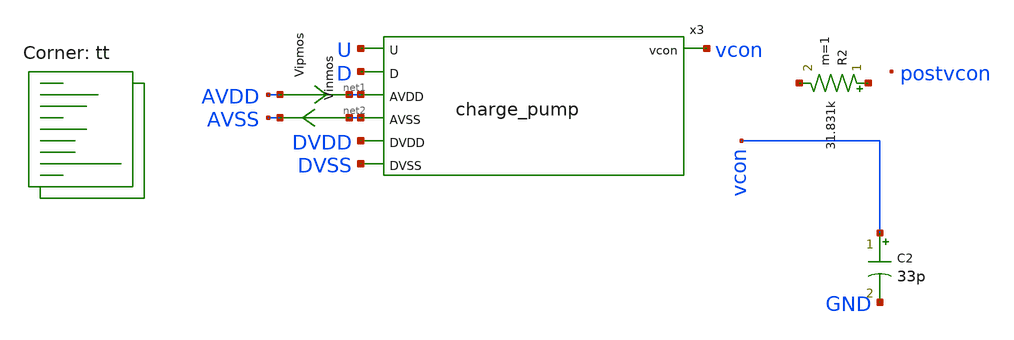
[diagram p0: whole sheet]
** sch_path: xschem/charge_pump-tb.sch
**.subckt charge_pump-tb
C2 vcon GND 33p m=1
R2 net3 net4 31.831k m=1
Vipmos AVDD net1 0
.save i(vipmos)
Vinmos net2 AVSS 0
.save i(vinmos)
x3 U D vcon net1 net2 DVDD DVSS charge_pump
**** begin user architecture code
 .lib $::SKYWATER_MODELS/sky130.lib.spice tt
.include $::SKYWATER_STDCELLS/sky130_fd_sc_hd.spice
.param mc_mm_switch = 0
.param mc_pr_switch = 0




  .param max_freq=100e6 period={1/max_freq} time_high={period/2}
  .param delay_vin1={time_high} delay_vin2={time_high*2}

  .option wnflag=1
  .option safecurrents

  Vvdd  AVDD AVSS dc 1.8
  Vavss AVSS GND  dc 0
  Vdvdd DVDD DVSS dc 1.8
  Vdvss DVSS GND  dc 0
  Vin1 U GND pulse(0 1.8 {delay_vin1} 1p 1p {time_high/3} {period})
  Vin2 D GND pulse(0 1.8 {delay_vin2} 1p 1p {time_high/3} {period})

  .control
     reset
     save all
     tran 0.01n 1u
     write charge_pump-tb.raw
     set appendwrite

     *alterparam lmos=0.54
     *reset
     *save all
     *tran 0.01n 500n
     *write charge_pump-tb.raw
    quit 0
  .endc



**** end user architecture code
**.ends

* expanding   symbol:  charge_pump.sym # of pins=7
** sym_path: xschem/charge_pump.sym
** sch_path: xschem/charge_pump.sch
.subckt charge_pump U D vcon AVDD AVSS DVDD DVSS
*.ipin U
*.ipin D
*.opin vcon
*.ipin AVDD
*.ipin AVSS
*.ipin DVDD
*.ipin DVSS
XM1 vcon Ub AVDD AVDD sky130_fd_pr__pfet_01v8 L=0.5 W=2.5 nf=1 ad='int((nf+1)/2) * W/nf * 0.29' as='int((nf+2)/2) * W/nf * 0.29'
+ pd='2*int((nf+1)/2) * (W/nf + 0.29)' ps='2*int((nf+2)/2) * (W/nf + 0.29)' nrd='0.29 / W' nrs='0.29 / W'
+ sa=0 sb=0 sd=0 mult=4 m=4
XM2 vcon net1 AVSS AVSS sky130_fd_pr__nfet_01v8 L=0.5 W=2.5 nf=1 ad='int((nf+1)/2) * W/nf * 0.29' as='int((nf+2)/2) * W/nf * 0.29'
+ pd='2*int((nf+1)/2) * (W/nf + 0.29)' ps='2*int((nf+2)/2) * (W/nf + 0.29)' nrd='0.29 / W' nrs='0.29 / W'
+ sa=0 sb=0 sd=0 mult=4 m=4
x1 D DVSS DVSS DVDD DVDD net1 sky130_fd_sc_hd__buf_1
x2 U DVSS DVSS DVDD DVDD Ub sky130_fd_sc_hd__inv_1
XM3 AVDD AVDD AVDD AVDD sky130_fd_pr__pfet_01v8 L=0.15 W=2.5 nf=1 ad='int((nf+1)/2) * W/nf * 0.29' as='int((nf+2)/2) * W/nf * 0.29'
+ pd='2*int((nf+1)/2) * (W/nf + 0.29)' ps='2*int((nf+2)/2) * (W/nf + 0.29)' nrd='0.29 / W' nrs='0.29 / W'
+ sa=0 sb=0 sd=0 mult=4 m=4
XM4 AVSS AVSS AVSS AVSS sky130_fd_pr__nfet_01v8 L=0.15 W=2.5 nf=1 ad='int((nf+1)/2) * W/nf * 0.29' as='int((nf+2)/2) * W/nf * 0.29'
+ pd='2*int((nf+1)/2) * (W/nf + 0.29)' ps='2*int((nf+2)/2) * (W/nf + 0.29)' nrd='0.29 / W' nrs='0.29 / W'
+ sa=0 sb=0 sd=0 mult=4 m=4
.ends

.end
